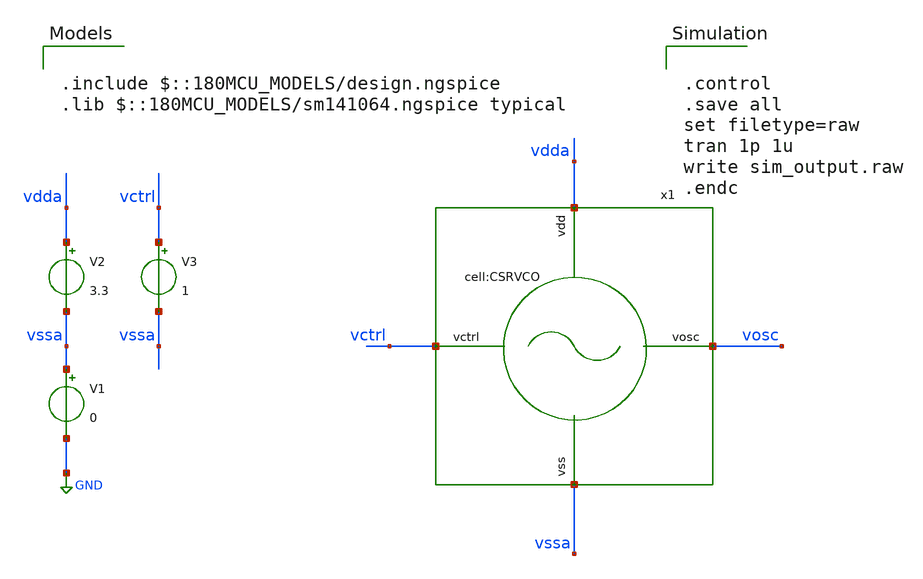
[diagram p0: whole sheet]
** sch_path: designs/libs/xp_tb_analog/tb_CSRVCO/tb_CSRVCO.sch
**.subckt tb_CSRVCO
x1 vctrl vdda vssa vosc CSRVCO
V1 vssa GND 0
V2 vdda vssa 3.3
V3 vctrl vssa 1
**** begin user architecture code

.include $::180MCU_MODELS/design.ngspice
.lib $::180MCU_MODELS/sm141064.ngspice typical



.control
.save all
set filetype=raw
tran 1p 1u
write sim_output.raw
.endc


**** end user architecture code
**.ends
.GLOBAL GND
.end
